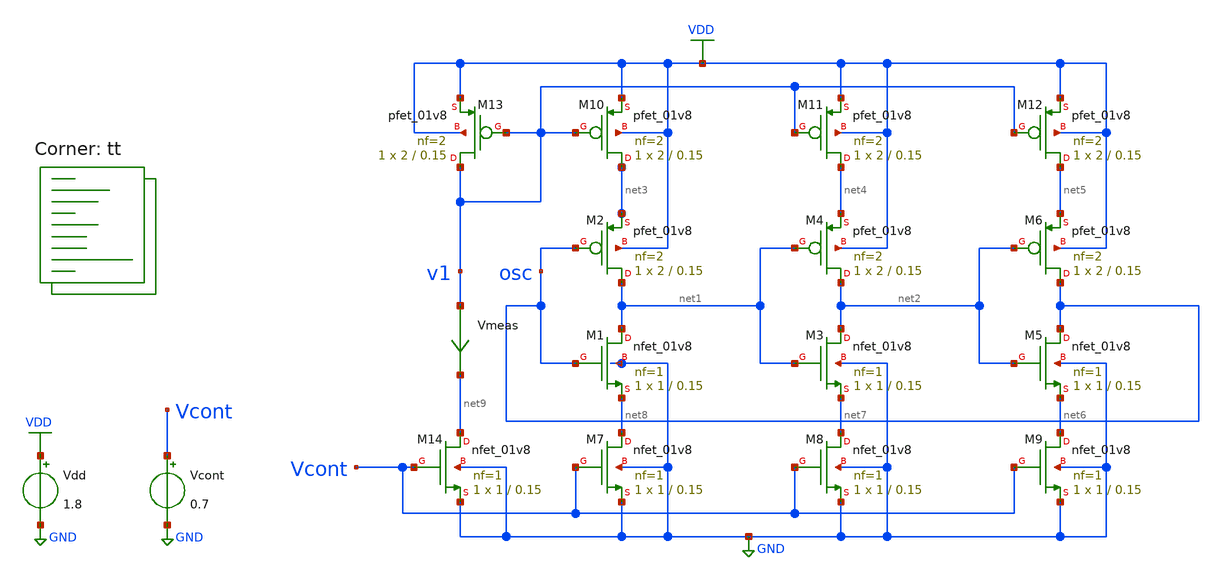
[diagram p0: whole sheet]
** sch_path: projects/pll/vco/xschem_ngspice/tb_current_starved_VCO.sch
**.subckt tb_current_starved_VCO
XM1 net1 osc net8 GND sky130_fd_pr__nfet_01v8 L=0.15 W=1 nf=1 ad='int((nf+1)/2) * W/nf * 0.29' as='int((nf+2)/2) * W/nf * 0.29'
+ pd='2*int((nf+1)/2) * (W/nf + 0.29)' ps='2*int((nf+2)/2) * (W/nf + 0.29)' nrd='0.29 / W' nrs='0.29 / W'
+ sa=0 sb=0 sd=0 mult=1 m=1
XM2 net1 osc net3 VDD sky130_fd_pr__pfet_01v8 L=0.15 W=2 nf=2 ad='int((nf+1)/2) * W/nf * 0.29' as='int((nf+2)/2) * W/nf * 0.29'
+ pd='2*int((nf+1)/2) * (W/nf + 0.29)' ps='2*int((nf+2)/2) * (W/nf + 0.29)' nrd='0.29 / W' nrs='0.29 / W'
+ sa=0 sb=0 sd=0 mult=1 m=1
XM3 net2 net1 net7 GND sky130_fd_pr__nfet_01v8 L=0.15 W=1 nf=1 ad='int((nf+1)/2) * W/nf * 0.29' as='int((nf+2)/2) * W/nf * 0.29'
+ pd='2*int((nf+1)/2) * (W/nf + 0.29)' ps='2*int((nf+2)/2) * (W/nf + 0.29)' nrd='0.29 / W' nrs='0.29 / W'
+ sa=0 sb=0 sd=0 mult=1 m=1
XM4 net2 net1 net4 VDD sky130_fd_pr__pfet_01v8 L=0.15 W=2 nf=2 ad='int((nf+1)/2) * W/nf * 0.29' as='int((nf+2)/2) * W/nf * 0.29'
+ pd='2*int((nf+1)/2) * (W/nf + 0.29)' ps='2*int((nf+2)/2) * (W/nf + 0.29)' nrd='0.29 / W' nrs='0.29 / W'
+ sa=0 sb=0 sd=0 mult=1 m=1
XM5 osc net2 net6 GND sky130_fd_pr__nfet_01v8 L=0.15 W=1 nf=1 ad='int((nf+1)/2) * W/nf * 0.29' as='int((nf+2)/2) * W/nf * 0.29'
+ pd='2*int((nf+1)/2) * (W/nf + 0.29)' ps='2*int((nf+2)/2) * (W/nf + 0.29)' nrd='0.29 / W' nrs='0.29 / W'
+ sa=0 sb=0 sd=0 mult=1 m=1
XM6 osc net2 net5 VDD sky130_fd_pr__pfet_01v8 L=0.15 W=2 nf=2 ad='int((nf+1)/2) * W/nf * 0.29' as='int((nf+2)/2) * W/nf * 0.29'
+ pd='2*int((nf+1)/2) * (W/nf + 0.29)' ps='2*int((nf+2)/2) * (W/nf + 0.29)' nrd='0.29 / W' nrs='0.29 / W'
+ sa=0 sb=0 sd=0 mult=1 m=1
XM7 net8 Vcont GND GND sky130_fd_pr__nfet_01v8 L=0.15 W=1 nf=1 ad='int((nf+1)/2) * W/nf * 0.29' as='int((nf+2)/2) * W/nf * 0.29'
+ pd='2*int((nf+1)/2) * (W/nf + 0.29)' ps='2*int((nf+2)/2) * (W/nf + 0.29)' nrd='0.29 / W' nrs='0.29 / W'
+ sa=0 sb=0 sd=0 mult=1 m=1
XM8 net7 Vcont GND GND sky130_fd_pr__nfet_01v8 L=0.15 W=1 nf=1 ad='int((nf+1)/2) * W/nf * 0.29' as='int((nf+2)/2) * W/nf * 0.29'
+ pd='2*int((nf+1)/2) * (W/nf + 0.29)' ps='2*int((nf+2)/2) * (W/nf + 0.29)' nrd='0.29 / W' nrs='0.29 / W'
+ sa=0 sb=0 sd=0 mult=1 m=1
XM9 net6 Vcont GND GND sky130_fd_pr__nfet_01v8 L=0.15 W=1 nf=1 ad='int((nf+1)/2) * W/nf * 0.29' as='int((nf+2)/2) * W/nf * 0.29'
+ pd='2*int((nf+1)/2) * (W/nf + 0.29)' ps='2*int((nf+2)/2) * (W/nf + 0.29)' nrd='0.29 / W' nrs='0.29 / W'
+ sa=0 sb=0 sd=0 mult=1 m=1
XM10 net3 v1 VDD VDD sky130_fd_pr__pfet_01v8 L=0.15 W=2 nf=2 ad='int((nf+1)/2) * W/nf * 0.29' as='int((nf+2)/2) * W/nf * 0.29'
+ pd='2*int((nf+1)/2) * (W/nf + 0.29)' ps='2*int((nf+2)/2) * (W/nf + 0.29)' nrd='0.29 / W' nrs='0.29 / W'
+ sa=0 sb=0 sd=0 mult=1 m=1
XM11 net4 v1 VDD VDD sky130_fd_pr__pfet_01v8 L=0.15 W=2 nf=2 ad='int((nf+1)/2) * W/nf * 0.29' as='int((nf+2)/2) * W/nf * 0.29'
+ pd='2*int((nf+1)/2) * (W/nf + 0.29)' ps='2*int((nf+2)/2) * (W/nf + 0.29)' nrd='0.29 / W' nrs='0.29 / W'
+ sa=0 sb=0 sd=0 mult=1 m=1
XM12 net5 v1 VDD VDD sky130_fd_pr__pfet_01v8 L=0.15 W=2 nf=2 ad='int((nf+1)/2) * W/nf * 0.29' as='int((nf+2)/2) * W/nf * 0.29'
+ pd='2*int((nf+1)/2) * (W/nf + 0.29)' ps='2*int((nf+2)/2) * (W/nf + 0.29)' nrd='0.29 / W' nrs='0.29 / W'
+ sa=0 sb=0 sd=0 mult=1 m=1
Vdd VDD GND 1.8
Vcont Vcont GND 0.7
XM13 v1 v1 VDD VDD sky130_fd_pr__pfet_01v8 L=0.15 W=2 nf=2 ad='int((nf+1)/2) * W/nf * 0.29' as='int((nf+2)/2) * W/nf * 0.29'
+ pd='2*int((nf+1)/2) * (W/nf + 0.29)' ps='2*int((nf+2)/2) * (W/nf + 0.29)' nrd='0.29 / W' nrs='0.29 / W'
+ sa=0 sb=0 sd=0 mult=1 m=1
XM14 net9 Vcont GND GND sky130_fd_pr__nfet_01v8 L=0.15 W=1 nf=1 ad='int((nf+1)/2) * W/nf * 0.29' as='int((nf+2)/2) * W/nf * 0.29'
+ pd='2*int((nf+1)/2) * (W/nf + 0.29)' ps='2*int((nf+2)/2) * (W/nf + 0.29)' nrd='0.29 / W' nrs='0.29 / W'
+ sa=0 sb=0 sd=0 mult=1 m=1
Vmeas v1 net9 0
.save i(vmeas)
**** begin user architecture code
.lib $::SKYWATER_MODELS/sky130.lib.spice tt



.option method=gear
.option wnflag=1


*.ic v(osc)=0

*.temp = 75

.control
  let v_cont_start = 0.0
  let v_cont_stop = 1.9

  dowhile v_cont_start <= v_cont_stop
    alter vcont $&v_cont_start
    save v(osc) v(vcont) v(v1)
    tran 2ps 30ns
    remzerovec
    write tb_current_starved_VCO_{$&v_cont_start}.raw
    *write tb_current_starved_VCO.raw
    let filename = v_cont_start * 100
    wrdata /foss/designs/my_design/projects/pll/vco/xschem_ngspice/tb_current_starved_VCO_{$&filename}.txt
+ v(osc)
    set appendwrite

    reset
    let v_cont_start = v_cont_start + 0.1
  end
.endc






**** end user architecture code
**.ends
.GLOBAL VDD
.GLOBAL GND
.end
